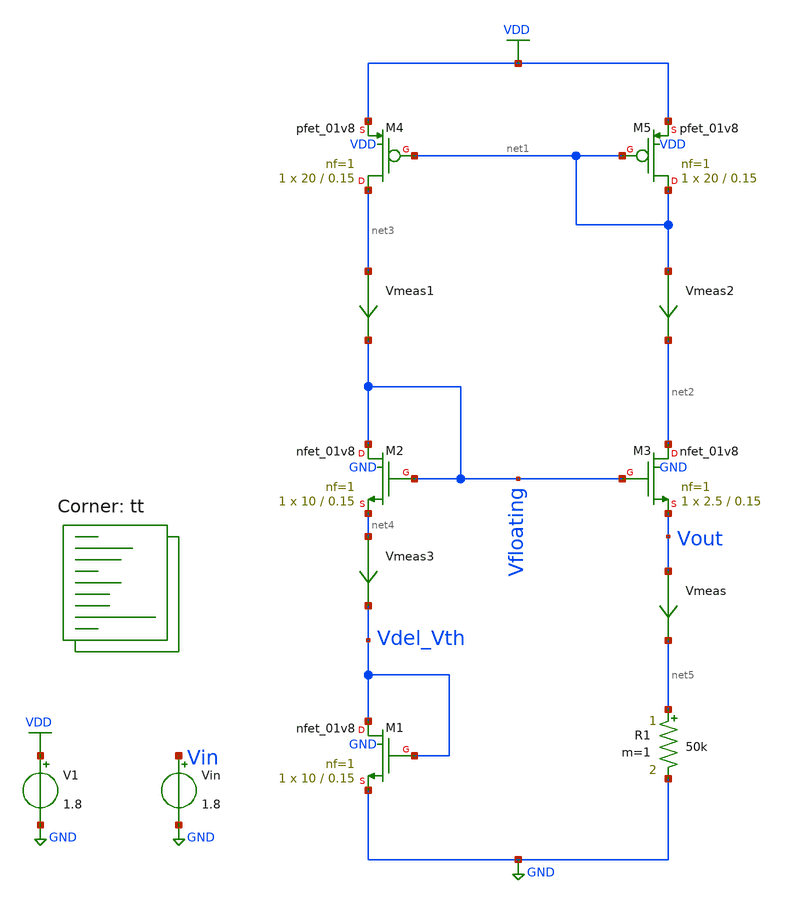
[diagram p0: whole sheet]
** sch_path: projects/pll/bandgapref/xschem_ngspice/mos_bandgap1.sch
**.subckt mos_bandgap1
XM1 Vdel_Vth Vdel_Vth GND GND sky130_fd_pr__nfet_01v8 L=0.15 W=10 nf=1 ad='int((nf+1)/2) * W/nf * 0.29'
+ as='int((nf+2)/2) * W/nf * 0.29' pd='2*int((nf+1)/2) * (W/nf + 0.29)' ps='2*int((nf+2)/2) * (W/nf + 0.29)'
+ nrd='0.29 / W' nrs='0.29 / W' sa=0 sb=0 sd=0 mult=1 m=1
XM2 Vfloating Vfloating net4 GND sky130_fd_pr__nfet_01v8 L=0.15 W=10 nf=1 ad='int((nf+1)/2) * W/nf * 0.29'
+ as='int((nf+2)/2) * W/nf * 0.29' pd='2*int((nf+1)/2) * (W/nf + 0.29)' ps='2*int((nf+2)/2) * (W/nf + 0.29)'
+ nrd='0.29 / W' nrs='0.29 / W' sa=0 sb=0 sd=0 mult=1 m=1
XM3 net2 Vfloating Vout GND sky130_fd_pr__nfet_01v8 L=0.15 W=2.5 nf=1 ad='int((nf+1)/2) * W/nf * 0.29'
+ as='int((nf+2)/2) * W/nf * 0.29' pd='2*int((nf+1)/2) * (W/nf + 0.29)' ps='2*int((nf+2)/2) * (W/nf + 0.29)'
+ nrd='0.29 / W' nrs='0.29 / W' sa=0 sb=0 sd=0 mult=1 m=1
XM4 net3 net1 VDD VDD sky130_fd_pr__pfet_01v8 L=0.15 W=20 nf=1 ad='int((nf+1)/2) * W/nf * 0.29' as='int((nf+2)/2) * W/nf * 0.29'
+ pd='2*int((nf+1)/2) * (W/nf + 0.29)' ps='2*int((nf+2)/2) * (W/nf + 0.29)' nrd='0.29 / W' nrs='0.29 / W'
+ sa=0 sb=0 sd=0 mult=1 m=1
XM5 net1 net1 VDD VDD sky130_fd_pr__pfet_01v8 L=0.15 W=20 nf=1 ad='int((nf+1)/2) * W/nf * 0.29' as='int((nf+2)/2) * W/nf * 0.29'
+ pd='2*int((nf+1)/2) * (W/nf + 0.29)' ps='2*int((nf+2)/2) * (W/nf + 0.29)' nrd='0.29 / W' nrs='0.29 / W'
+ sa=0 sb=0 sd=0 mult=1 m=1
V1 VDD GND 1.8
R1 net5 GND 50k m=1
Vin Vin GND 1.8
Vmeas Vout net5 0
.save i(vmeas)
Vmeas1 net3 Vfloating 0
.save i(vmeas1)
Vmeas2 net1 net2 0
.save i(vmeas2)
Vmeas3 net4 Vdel_Vth 0
.save i(vmeas3)
**** begin user architecture code
.lib $::SKYWATER_MODELS/sky130.lib.spice tt



.option wnflag=1

.param VDDGAUSS = agauss(1.8, 0.05, 1)
.param VDD = VDDGAUSS
* .param VDD = 1.8

.param TEMPGAUSS = agauss(40, 30, 1)
.param temp = TEMPGAUSS
* .option temp = 25

.control

  option seed=9
  let run=0
  dowhile run <= 20
    save all
    dc Vin 0 1.8 0.2
    remzerovec
    write mos_bandgap1.raw
    set appendwrite
    reset
    let run = run + 1
  end

.endc



**** end user architecture code
**.ends
.GLOBAL GND
.GLOBAL VDD
.end
